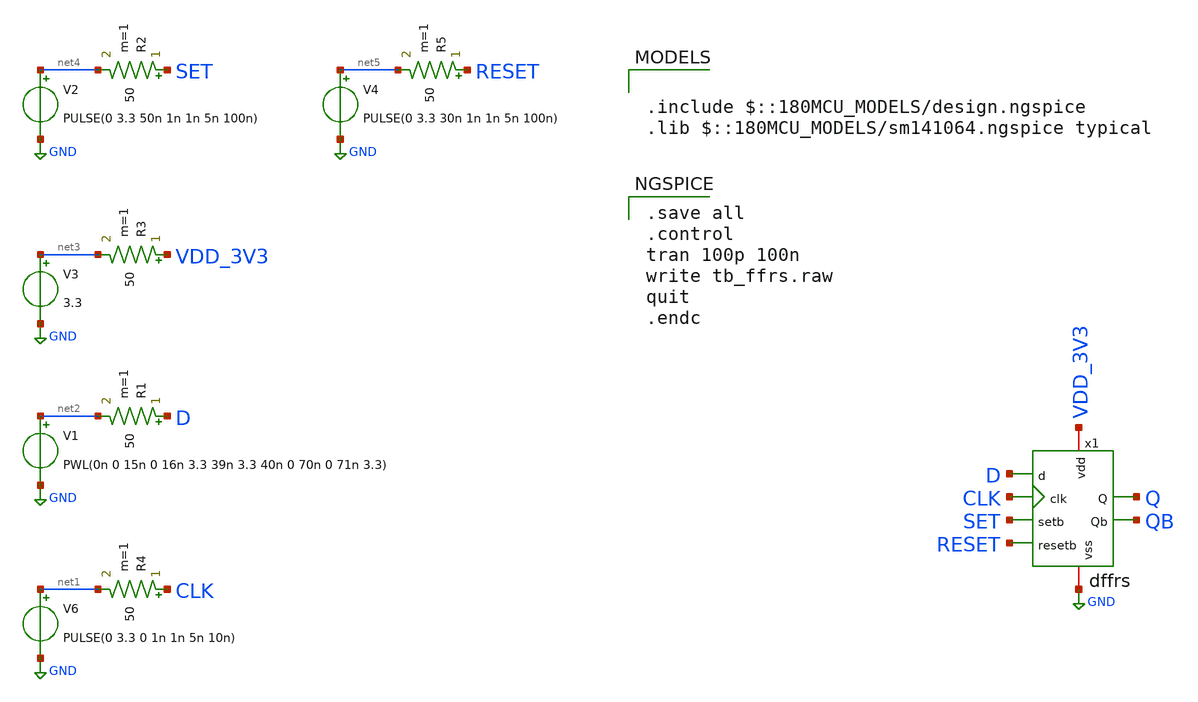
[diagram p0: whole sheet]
** sch_path: designs/libs/tspc_flip_flop/tspc_flip_flop_tb.sch
**.subckt tspc_flip_flop_tb
V6 net1 GND PULSE(0 3.3 0 1n 1n 5n 10n)
R4 CLK net1 50 m=1
V1 net2 GND PWL(0n 0 15n 0 16n 3.3 39n 3.3 40n 0 70n 0 71n 3.3)
R1 D net2 50 m=1
V3 net3 GND 3.3
R3 VDD_3V3 net3 50 m=1
V2 net4 GND PULSE(0 3.3 50n 1n 1n 5n 100n)
R2 SET net4 50 m=1
V4 net5 GND PULSE(0 3.3 30n 1n 1n 5n 100n)
R5 RESET net5 50 m=1
x1 VDD_3V3 GND D CLK SET RESET Q QB dffrs
**** begin user architecture code

.include $::180MCU_MODELS/design.ngspice
.lib $::180MCU_MODELS/sm141064.ngspice typical


.save all
.control
tran 100p 100n
write tb_ffrs.raw
quit
.endc

**** end user architecture code
**.ends
.GLOBAL GND
.end
